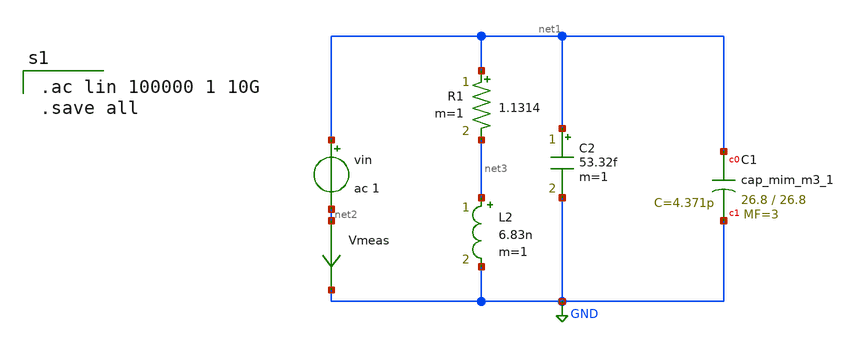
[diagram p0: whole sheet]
** sch_path: XSCHEM/ANTENNA/RLC_CSTXschem300.sch
**.subckt RLC_CSTXschem300
vin net1 net2 ac 1
XC1 net1 GND sky130_fd_pr__cap_mim_m3_1 W=26.8 L=26.8 MF=3 m=3
Vmeas net2 GND 0
.save i(vmeas)
R1 net1 net3 1.1314 m=1
L2 net3 GND 6.83n m=1
C2 net1 GND 53.32f m=1
**** begin user architecture code

.ac lin 100000 1 10G
.save all


** opencircuitdesign pdks install
.lib $::SKYWATER_MODELS/sky130.lib.spice ff
.include /usr/local/share/pdk/sky130A/libs.ref/sky130_fd_sc_hd/spice/sky130_fd_sc_hd.spice

**** end user architecture code
**.ends
.GLOBAL GND
.end
